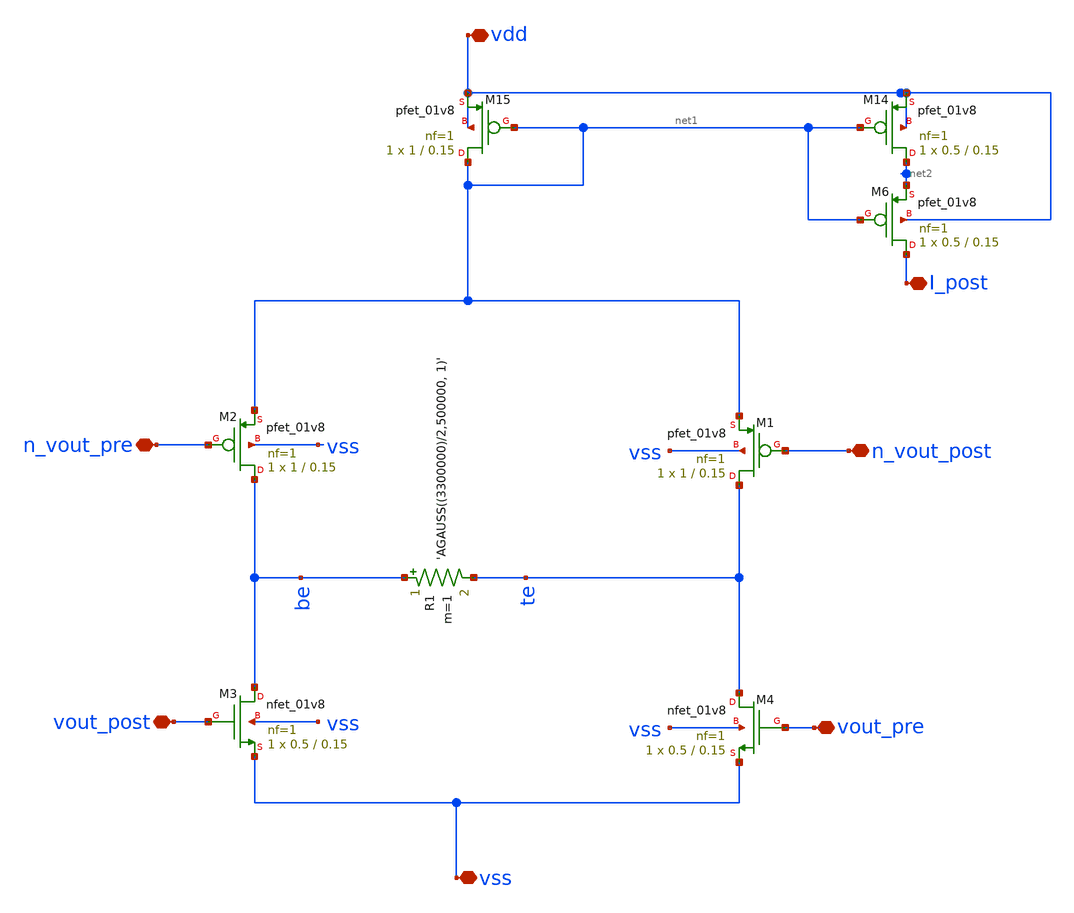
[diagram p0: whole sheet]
** sch_path: Synapse/no_stdp.sch
**.subckt no_stdp vdd vss vout_post vout_pre I_post n_vout_post n_vout_pre
*.iopin vdd
*.iopin vss
*.iopin vout_post
*.iopin vout_pre
*.iopin I_post
*.iopin n_vout_post
*.iopin n_vout_pre
XM3 be vout_post vss vss sky130_fd_pr__nfet_01v8 L=0.15 W=0.5 nf=1 ad='int((nf+1)/2) * W/nf * 0.29' as='int((nf+2)/2) * W/nf * 0.29'
+ pd='2*int((nf+1)/2) * (W/nf + 0.29)' ps='2*int((nf+2)/2) * (W/nf + 0.29)' nrd='0.29 / W' nrs='0.29 / W'
+ sa=0 sb=0 sd=0 mult=1 m=1
XM4 te vout_pre vss vss sky130_fd_pr__nfet_01v8 L=0.15 W=0.5 nf=1 ad='int((nf+1)/2) * W/nf * 0.29' as='int((nf+2)/2) * W/nf * 0.29'
+ pd='2*int((nf+1)/2) * (W/nf + 0.29)' ps='2*int((nf+2)/2) * (W/nf + 0.29)' nrd='0.29 / W' nrs='0.29 / W'
+ sa=0 sb=0 sd=0 mult=1 m=1
XM14 net2 net1 vdd vdd sky130_fd_pr__pfet_01v8 L=0.15 W=0.5 nf=1 ad='int((nf+1)/2) * W/nf * 0.29' as='int((nf+2)/2) * W/nf * 0.29'
+ pd='2*int((nf+1)/2) * (W/nf + 0.29)' ps='2*int((nf+2)/2) * (W/nf + 0.29)' nrd='0.29 / W' nrs='0.29 / W'
+ sa=0 sb=0 sd=0 mult=1 m=1
XM15 net1 net1 vdd vdd sky130_fd_pr__pfet_01v8 L=0.15 W=1 nf=1 ad='int((nf+1)/2) * W/nf * 0.29' as='int((nf+2)/2) * W/nf * 0.29'
+ pd='2*int((nf+1)/2) * (W/nf + 0.29)' ps='2*int((nf+2)/2) * (W/nf + 0.29)' nrd='0.29 / W' nrs='0.29 / W'
+ sa=0 sb=0 sd=0 mult=1 m=1
XM1 te n_vout_post net1 vss sky130_fd_pr__pfet_01v8 L=0.15 W=1 nf=1 ad='int((nf+1)/2) * W/nf * 0.29'
+ as='int((nf+2)/2) * W/nf * 0.29' pd='2*int((nf+1)/2) * (W/nf + 0.29)' ps='2*int((nf+2)/2) * (W/nf + 0.29)'
+ nrd='0.29 / W' nrs='0.29 / W' sa=0 sb=0 sd=0 mult=1 m=1
XM2 be n_vout_pre net1 vss sky130_fd_pr__pfet_01v8 L=0.15 W=1 nf=1 ad='int((nf+1)/2) * W/nf * 0.29' as='int((nf+2)/2) * W/nf * 0.29'
+ pd='2*int((nf+1)/2) * (W/nf + 0.29)' ps='2*int((nf+2)/2) * (W/nf + 0.29)' nrd='0.29 / W' nrs='0.29 / W'
+ sa=0 sb=0 sd=0 mult=1 m=1
XM6 I_post net1 net2 vdd sky130_fd_pr__pfet_01v8 L=0.15 W=0.5 nf=1 ad='int((nf+1)/2) * W/nf * 0.29' as='int((nf+2)/2) * W/nf * 0.29'
+ pd='2*int((nf+1)/2) * (W/nf + 0.29)' ps='2*int((nf+2)/2) * (W/nf + 0.29)' nrd='0.29 / W' nrs='0.29 / W'
+ sa=0 sb=0 sd=0 mult=1 m=1
R1 be te 'AGAUSS((3300000)/2,500000, 1)' m=1
**.ends
.end
